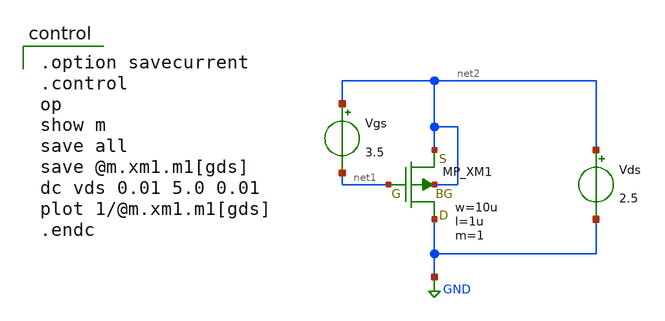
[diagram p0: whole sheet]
** sch_path: TR10/opamp/ibias_rds.sch
**.subckt ibias_rds
Vgs net2 net1 3.5
Vds net2 GND 2.5
XM1 GND net1 net2 net2 PMOS w=10u l=1u as=0 ad=0 ps=0 pd=0 nrd=0 nrs=0 m=1
**** begin user architecture code

.option savecurrent
.control
op
show m
save all
save @m.xm1.m1[gds]
dc vds 0.01 5.0 0.01
plot 1/@m.xm1.m1[gds]
.endc

 .include $::LIB/../ip62_models
**** end user architecture code
**.ends
.GLOBAL GND
.end
